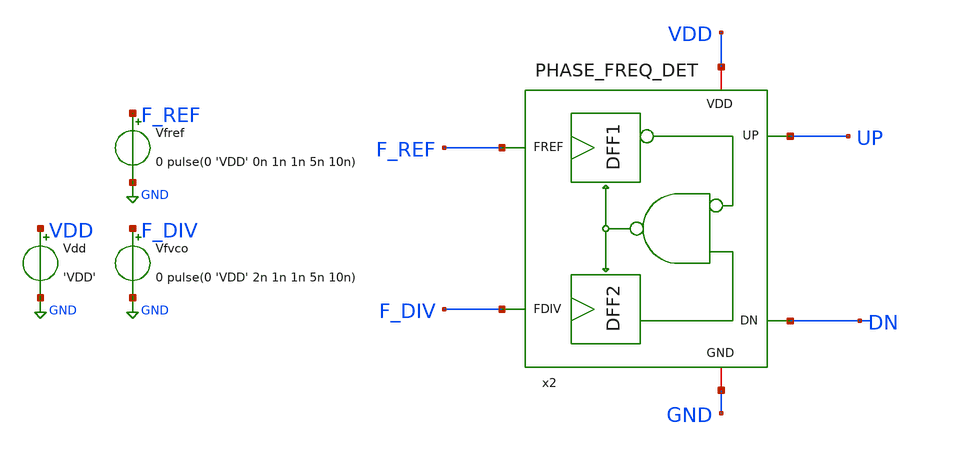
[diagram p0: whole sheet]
** sch_path: xschem/phase-freq-detector/tb_PHASE_FREQ_DET.sch
**.subckt tb_PHASE_FREQ_DET
Vdd VDD GND 'VDD'
Vfvco F_DIV GND 0 pulse(0 'VDD' 2n 1n 1n 5n 10n)
Vfref F_REF GND 0 pulse(0 'VDD' 0n 1n 1n 5n 10n)
x2 F_REF UP VDD GND F_DIV DN PHASE_FREQ_DET
**** begin user architecture code



.param RAW_TEMP = agauss(40, 30, 1)
.param TEMPGAUSS = max(20, min(RAW_TEMP, 80))
.option temp = 'TEMPGAUSS'
.param VDDGAUSS = agauss(1.2, 0.05, 1)

.param VDD = 'VDDGAUSS'
* analysis

.tran 100p 30n uic

.control
let i = 0
dowhile i < 10
  reset
  run
  write tb_PHASE_FREQ_DET.raw
  set appendwrite
  reset
  let i = i + 1
end
quit
.endc






.lib cornerMOSlv.lib mos_tt
.lib cornerMOShv.lib mos_tt
.lib cornerHBT.lib hbt_typ
.lib cornerRES.lib res_typ
.include /foss/pdks/ihp-sg13g2/libs.ref/sg13g2_stdcell/spice/sg13g2_stdcell.spice
.global VDD GND




**** end user architecture code
**.ends

* expanding   symbol:  xschem/phase-freq-detector/PHASE_FREQ_DET.sym # of pins=6
** sym_path: xschem/phase-freq-detector/PHASE_FREQ_DET.sym
** sch_path: xschem/phase-freq-detector/PHASE_FREQ_DET.sch
.subckt PHASE_FREQ_DET FREF UP VDD GND FDIV DN
*.opin UP
*.ipin FREF
*.iopin VDD
*.iopin GND
*.opin DN
*.ipin FDIV
x1 net1 UP FREF VDD nRST VDD GND sg13g2_dfrbp_2
x2 DN net2 FDIV VDD nRST VDD GND sg13g2_dfrbp_2
x3 nRST net1 DN VDD GND sg13g2_nand2_2
* noconn #net2
.ends

.GLOBAL GND
.GLOBAL VDD
.end
